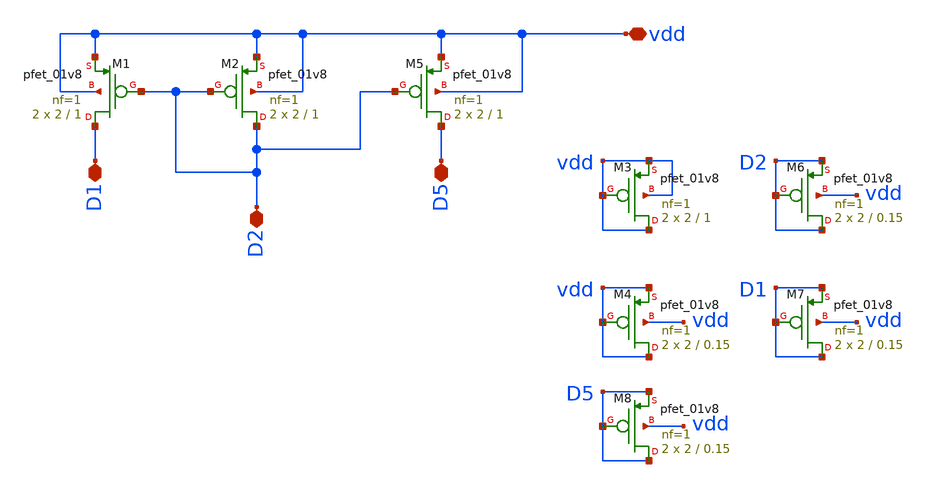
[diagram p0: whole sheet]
** sch_path: pmoscs.sch
**.subckt pmoscs vdd D1 D2 D5
*.iopin vdd
*.iopin D1
*.iopin D2
*.iopin D5
XM1 D1 D2 vdd vdd sky130_fd_pr__pfet_01v8 L=1 W=2 nf=1 ad='int((nf+1)/2) * W/nf * 0.29' as='int((nf+2)/2) * W/nf * 0.29'
+ pd='2*int((nf+1)/2) * (W/nf + 0.29)' ps='2*int((nf+2)/2) * (W/nf + 0.29)' nrd='0.29 / W' nrs='0.29 / W'
+ sa=0 sb=0 sd=0 mult=2 m=2
XM2 D2 D2 vdd vdd sky130_fd_pr__pfet_01v8 L=1 W=2 nf=1 ad='int((nf+1)/2) * W/nf * 0.29' as='int((nf+2)/2) * W/nf * 0.29'
+ pd='2*int((nf+1)/2) * (W/nf + 0.29)' ps='2*int((nf+2)/2) * (W/nf + 0.29)' nrd='0.29 / W' nrs='0.29 / W'
+ sa=0 sb=0 sd=0 mult=2 m=2
XM5 D5 D2 vdd vdd sky130_fd_pr__pfet_01v8 L=1 W=2 nf=1 ad='int((nf+1)/2) * W/nf * 0.29' as='int((nf+2)/2) * W/nf * 0.29'
+ pd='2*int((nf+1)/2) * (W/nf + 0.29)' ps='2*int((nf+2)/2) * (W/nf + 0.29)' nrd='0.29 / W' nrs='0.29 / W'
+ sa=0 sb=0 sd=0 mult=2 m=2
XM3 vdd vdd vdd vdd sky130_fd_pr__pfet_01v8 L=1 W=2 nf=1 ad='int((nf+1)/2) * W/nf * 0.29' as='int((nf+2)/2) * W/nf * 0.29'
+ pd='2*int((nf+1)/2) * (W/nf + 0.29)' ps='2*int((nf+2)/2) * (W/nf + 0.29)' nrd='0.29 / W' nrs='0.29 / W'
+ sa=0 sb=0 sd=0 mult=2 m=2
XM4 vdd vdd vdd vdd sky130_fd_pr__pfet_01v8 L=0.15 W=2 nf=1 ad='int((nf+1)/2) * W/nf * 0.29' as='int((nf+2)/2) * W/nf * 0.29'
+ pd='2*int((nf+1)/2) * (W/nf + 0.29)' ps='2*int((nf+2)/2) * (W/nf + 0.29)' nrd='0.29 / W' nrs='0.29 / W'
+ sa=0 sb=0 sd=0 mult=2 m=2
XM6 D2 D2 D2 vdd sky130_fd_pr__pfet_01v8 L=0.15 W=2 nf=1 ad='int((nf+1)/2) * W/nf * 0.29' as='int((nf+2)/2) * W/nf * 0.29'
+ pd='2*int((nf+1)/2) * (W/nf + 0.29)' ps='2*int((nf+2)/2) * (W/nf + 0.29)' nrd='0.29 / W' nrs='0.29 / W'
+ sa=0 sb=0 sd=0 mult=2 m=2
XM7 D1 D1 D1 vdd sky130_fd_pr__pfet_01v8 L=0.15 W=2 nf=1 ad='int((nf+1)/2) * W/nf * 0.29' as='int((nf+2)/2) * W/nf * 0.29'
+ pd='2*int((nf+1)/2) * (W/nf + 0.29)' ps='2*int((nf+2)/2) * (W/nf + 0.29)' nrd='0.29 / W' nrs='0.29 / W'
+ sa=0 sb=0 sd=0 mult=2 m=2
XM8 D5 D5 D5 vdd sky130_fd_pr__pfet_01v8 L=0.15 W=2 nf=1 ad='int((nf+1)/2) * W/nf * 0.29' as='int((nf+2)/2) * W/nf * 0.29'
+ pd='2*int((nf+1)/2) * (W/nf + 0.29)' ps='2*int((nf+2)/2) * (W/nf + 0.29)' nrd='0.29 / W' nrs='0.29 / W'
+ sa=0 sb=0 sd=0 mult=2 m=2
**.ends
.end
